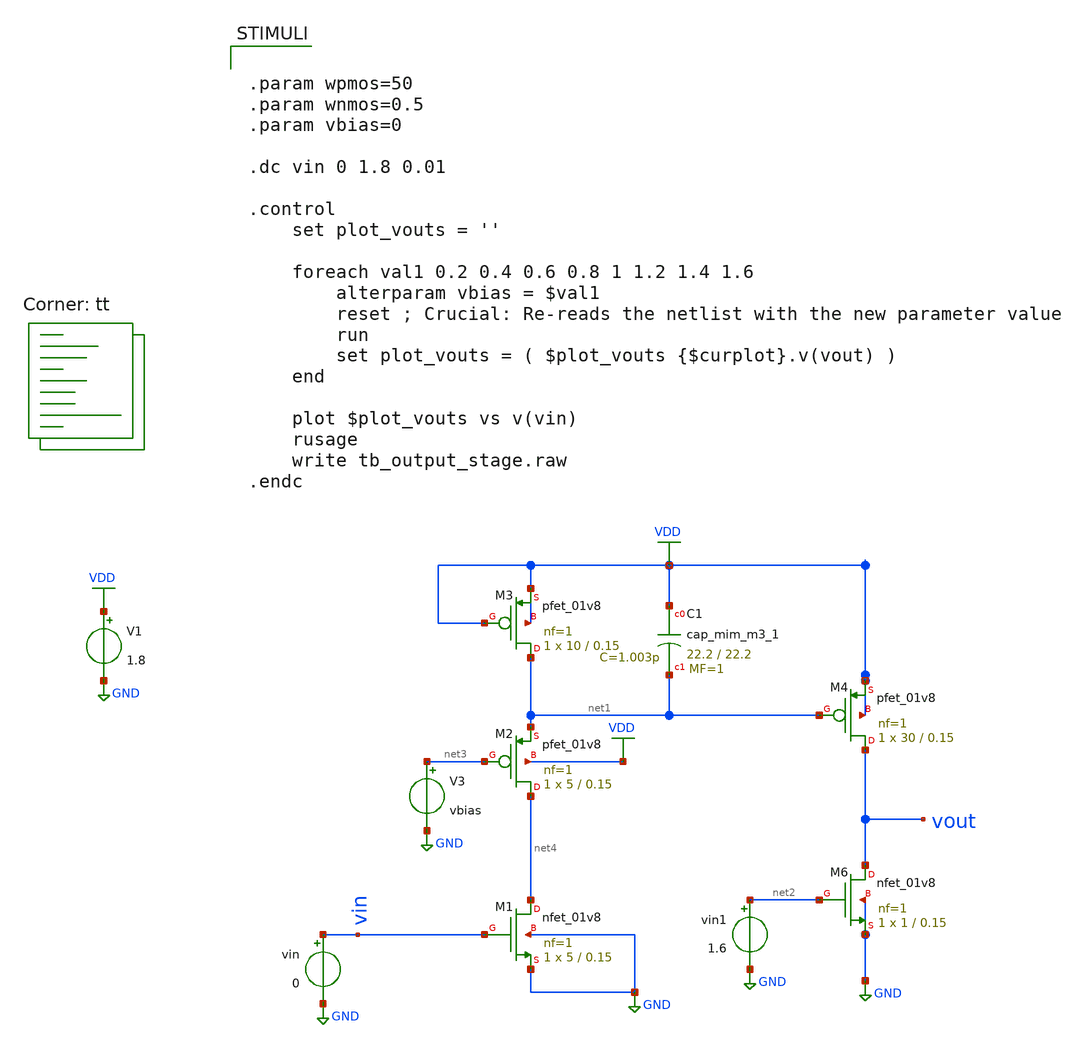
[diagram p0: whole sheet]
** sch_path: Neuron/ultralif/tb_output_stage.sch
**.subckt tb_output_stage
XM4 vout net1 VDD VDD sky130_fd_pr__pfet_01v8 L=0.15 W=30 nf=1 ad='int((nf+1)/2) * W/nf * 0.29' as='int((nf+2)/2) * W/nf * 0.29'
+ pd='2*int((nf+1)/2) * (W/nf + 0.29)' ps='2*int((nf+2)/2) * (W/nf + 0.29)' nrd='0.29 / W' nrs='0.29 / W'
+ sa=0 sb=0 sd=0 mult=1 m=1
XM6 vout net2 GND GND sky130_fd_pr__nfet_01v8 L=0.15 W=1 nf=1 ad='int((nf+1)/2) * W/nf * 0.29' as='int((nf+2)/2) * W/nf * 0.29'
+ pd='2*int((nf+1)/2) * (W/nf + 0.29)' ps='2*int((nf+2)/2) * (W/nf + 0.29)' nrd='0.29 / W' nrs='0.29 / W'
+ sa=0 sb=0 sd=0 mult=1 m=1
V1 VDD GND 1.8
vin vin GND 0
vin1 net2 GND 1.6
XM1 net4 vin GND GND sky130_fd_pr__nfet_01v8 L=0.15 W=5 nf=1 ad='int((nf+1)/2) * W/nf * 0.29' as='int((nf+2)/2) * W/nf * 0.29'
+ pd='2*int((nf+1)/2) * (W/nf + 0.29)' ps='2*int((nf+2)/2) * (W/nf + 0.29)' nrd='0.29 / W' nrs='0.29 / W'
+ sa=0 sb=0 sd=0 mult=1 m=1
XM2 net4 net3 net1 VDD sky130_fd_pr__pfet_01v8 L=0.15 W=5 nf=1 ad='int((nf+1)/2) * W/nf * 0.29' as='int((nf+2)/2) * W/nf * 0.29'
+ pd='2*int((nf+1)/2) * (W/nf + 0.29)' ps='2*int((nf+2)/2) * (W/nf + 0.29)' nrd='0.29 / W' nrs='0.29 / W'
+ sa=0 sb=0 sd=0 mult=1 m=1
XM3 net1 VDD VDD VDD sky130_fd_pr__pfet_01v8 L=0.15 W=10 nf=1 ad='int((nf+1)/2) * W/nf * 0.29' as='int((nf+2)/2) * W/nf * 0.29'
+ pd='2*int((nf+1)/2) * (W/nf + 0.29)' ps='2*int((nf+2)/2) * (W/nf + 0.29)' nrd='0.29 / W' nrs='0.29 / W'
+ sa=0 sb=0 sd=0 mult=1 m=1
V3 net3 GND vbias
XC1 VDD net1 sky130_fd_pr__cap_mim_m3_1 W=22.2 L=22.2 MF=1 m=1
**** begin user architecture code
.lib $::SKYWATER_MODELS/sky130.lib.spice tt
**** end user architecture code
**.ends
.GLOBAL GND
.GLOBAL VDD
**** begin user architecture code


.param wpmos=50
.param wnmos=0.5
.param vbias=0

.dc vin 0 1.8 0.01

.control
    set plot_vouts = ''

    foreach val1 0.2 0.4 0.6 0.8 1 1.2 1.4 1.6
        alterparam vbias = $val1
        reset ; Crucial: Re-reads the netlist with the new parameter value
        run
        set plot_vouts = ( $plot_vouts {$curplot}.v(vout) )
    end

    plot $plot_vouts vs v(vin)
    rusage
    write tb_output_stage.raw
.endc


**** end user architecture code
.end
